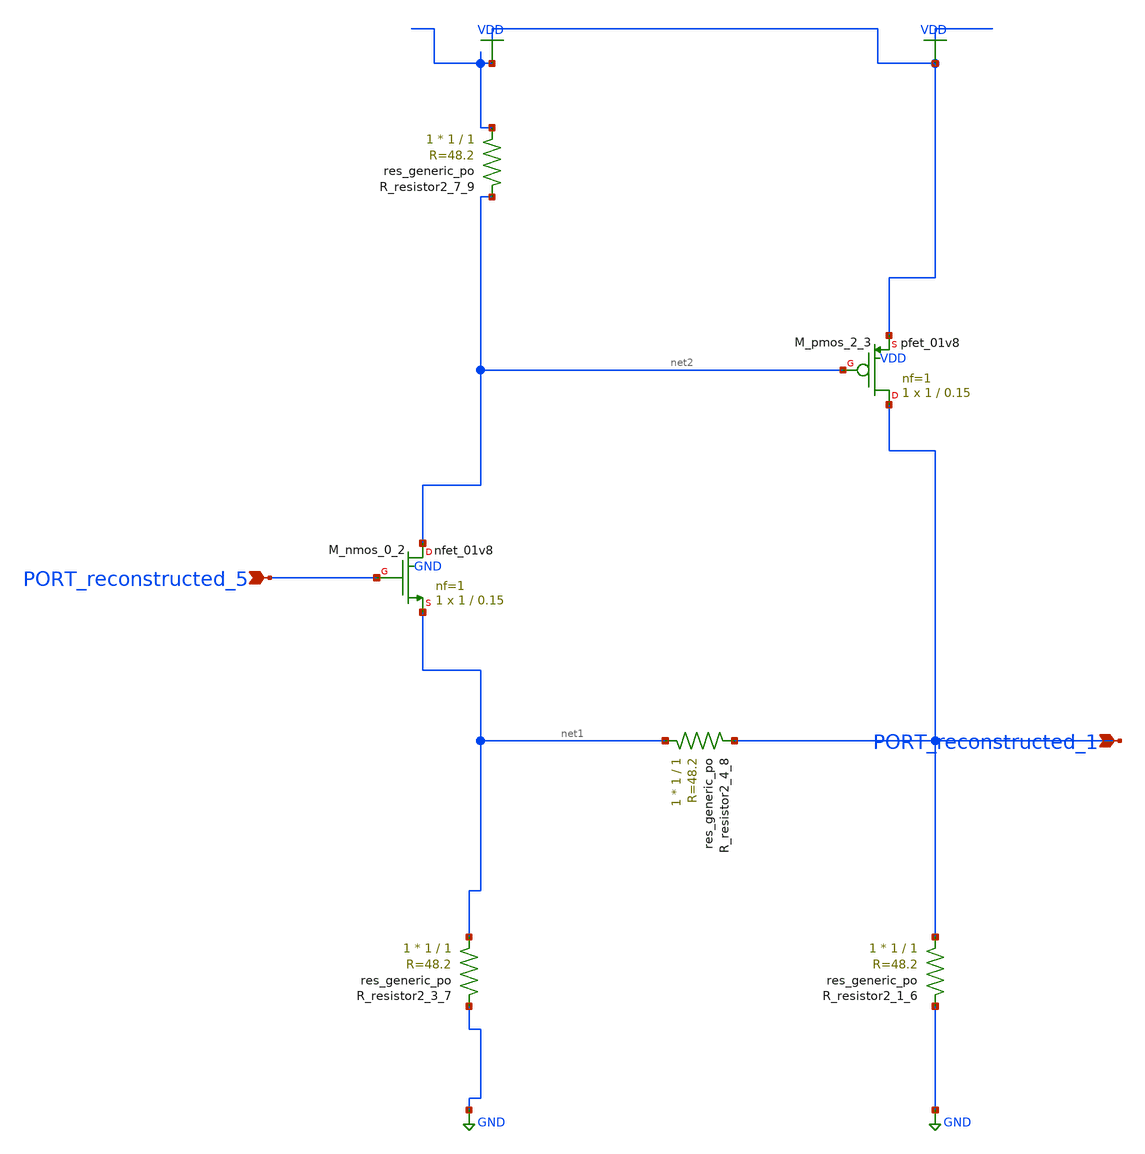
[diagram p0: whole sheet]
** sch_path: schematics/AMSNet/576.sch
**.subckt 576 PORT_reconstructed_5 PORT_reconstructed_1
*.ipin PORT_reconstructed_5
*.ipin PORT_reconstructed_1
XM_nmos_0_2 net2 PORT_reconstructed_5 net1 GND sky130_fd_pr__nfet_01v8 L=0.15 W=1 nf=1 ad='int((1 + 1)/2) * 1 / 1 * 0.29'
+ as='int((1 + 2)/2) * 1 / 1 * 0.29' pd='2*int((1 + 1)/2) * (1 / 1 + 0.29)' ps='2*int((1 + 2)/2) * (1 / 1 + 0.29)'
+ nrd='0.29 / 1 ' nrs='0.29 / 1 ' sa=0 sb=0 sd=0 mult=1 m=1
XM_pmos_2_3 PORT_reconstructed_1 net2 VDD VDD sky130_fd_pr__pfet_01v8 L=0.15 W=1 nf=1 ad='int((1 + 1)/2) * 1 / 1 * 0.29'
+ as='int((1 + 2)/2) * 1 / 1 * 0.29' pd='2*int((1 + 1)/2) * (1 / 1 + 0.29)' ps='2*int((1 + 2)/2) * (1 / 1 + 0.29)'
+ nrd='0.29 / 1 ' nrs='0.29 / 1 ' sa=0 sb=0 sd=0 mult=1 m=1
XR_resistor2_1_6 PORT_reconstructed_1 GND sky130_fd_pr__res_generic_po W=1 L=1 m=1
XR_resistor2_3_7 net1 GND sky130_fd_pr__res_generic_po W=1 L=1 m=1
XR_resistor2_4_8 net1 PORT_reconstructed_1 sky130_fd_pr__res_generic_po W=1 L=1 m=1
XR_resistor2_7_9 VDD net2 sky130_fd_pr__res_generic_po W=1 L=1 m=1
**.ends
.GLOBAL GND
.GLOBAL VDD
.end
